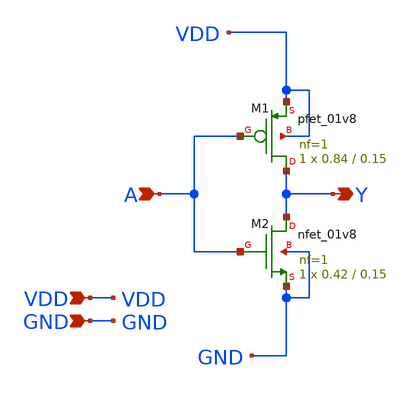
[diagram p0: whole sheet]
** sch_path: Adder/xschem/inv.sch
**.subckt inv Y A VDD GND
*.opin Y
*.ipin A
*.ipin VDD
*.ipin GND
XM1 Y A VDD VDD sky130_fd_pr__pfet_01v8 L=0.15 W=0.84 nf=1 ad='int((nf+1)/2) * W/nf * 0.29' as='int((nf+2)/2) * W/nf * 0.29'
+ pd='2*int((nf+1)/2) * (W/nf + 0.29)' ps='2*int((nf+2)/2) * (W/nf + 0.29)' nrd='0.29 / W' nrs='0.29 / W'
+ sa=0 sb=0 sd=0 mult=1 m=1
XM2 Y A GND GND sky130_fd_pr__nfet_01v8 L=0.15 W=0.42 nf=1 ad='int((nf+1)/2) * W/nf * 0.29' as='int((nf+2)/2) * W/nf * 0.29'
+ pd='2*int((nf+1)/2) * (W/nf + 0.29)' ps='2*int((nf+2)/2) * (W/nf + 0.29)' nrd='0.29 / W' nrs='0.29 / W'
+ sa=0 sb=0 sd=0 mult=1 m=1
**.ends
.end
